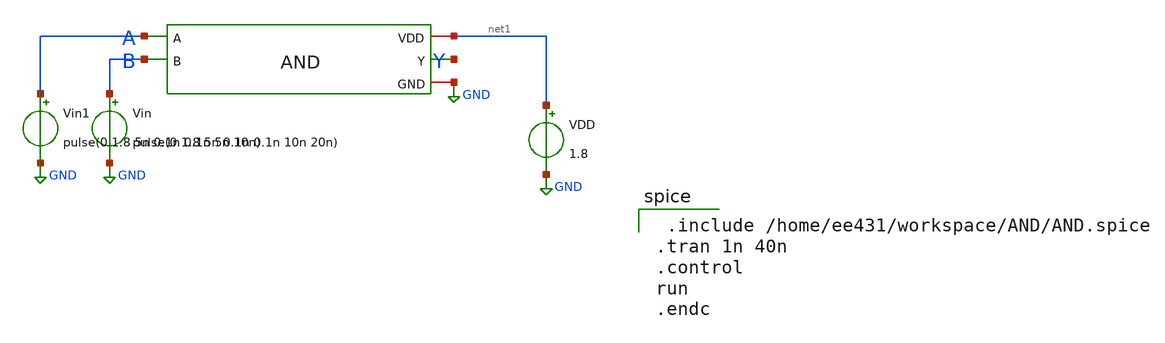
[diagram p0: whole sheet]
** sch_path: AND/AND_Testbench.sch
**.subckt AND_Testbench
x1 A B net1 Y GND AND
Vin B GND pulse(0 1.8 5n 0.1n 0.1n 10n 20n)
Vin1 A GND pulse(0 1.8 5n 0.1n 0.1n 5n 10n)
VDD net1 GND 1.8
**** begin user architecture code

.lib /usr/local/share/pdk/sky130A/libs.tech/ngspice/sky130.lib.spice tt


 .include /home/ee431/workspace/AND/AND.spice
.tran 1n 40n
.control
run
.endc

**** end user architecture code
**.ends
.GLOBAL GND
.end
